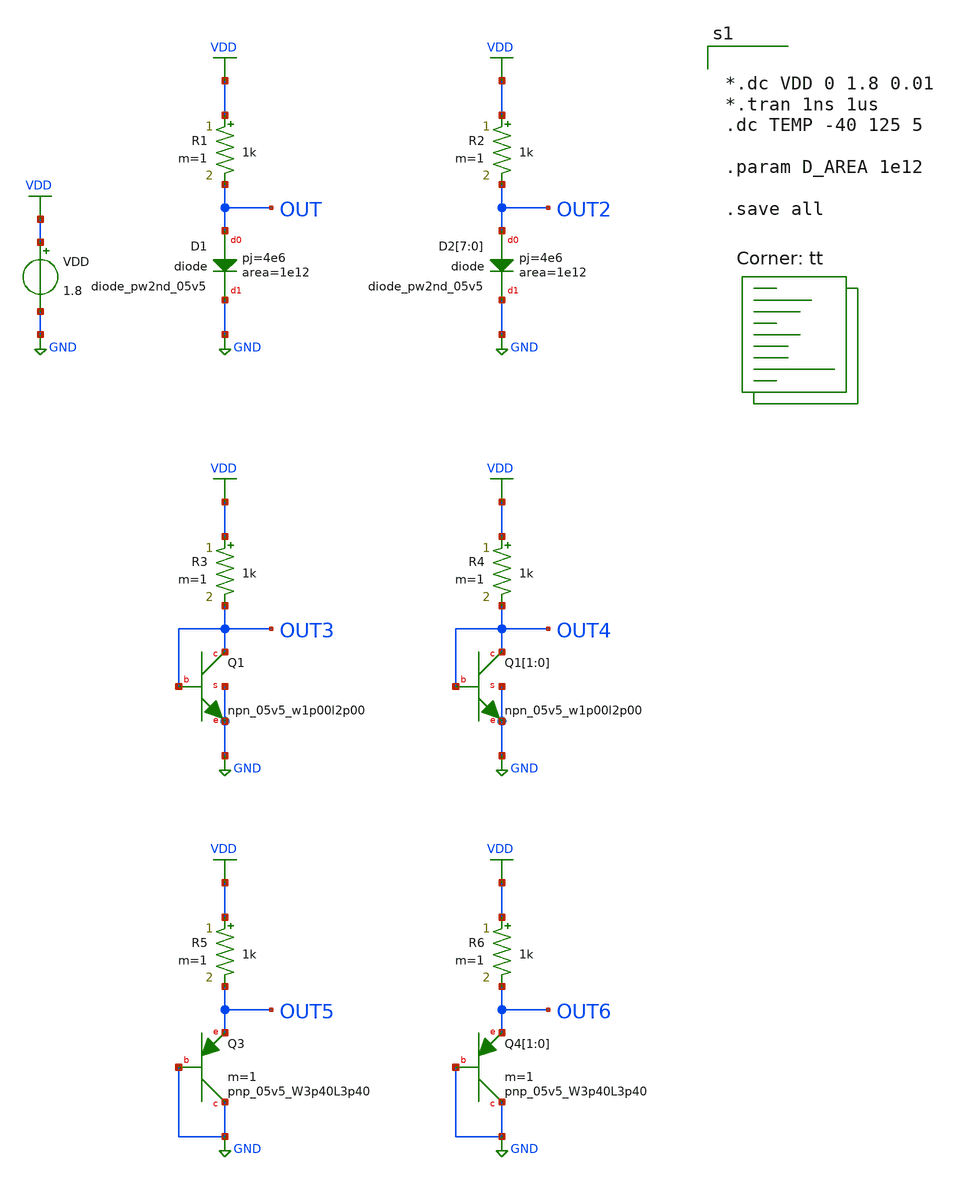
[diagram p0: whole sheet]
** sch_path: design/CNR_GR04_SKY130NM/CNR_GR04_Temp_Sweep.sch
**.subckt CNR_GR04_Temp_Sweep
XD1 OUT GND sky130_fd_pr__diode_pw2nd_05v5 area=1e12 pj=4e6
R1 VDD OUT 1k m=1
VDD VDD GND 1.8
XD2[7] OUT2 GND sky130_fd_pr__diode_pw2nd_05v5 area=1e12 pj=4e6
XD2[6] OUT2 GND sky130_fd_pr__diode_pw2nd_05v5 area=1e12 pj=4e6
XD2[5] OUT2 GND sky130_fd_pr__diode_pw2nd_05v5 area=1e12 pj=4e6
XD2[4] OUT2 GND sky130_fd_pr__diode_pw2nd_05v5 area=1e12 pj=4e6
XD2[3] OUT2 GND sky130_fd_pr__diode_pw2nd_05v5 area=1e12 pj=4e6
XD2[2] OUT2 GND sky130_fd_pr__diode_pw2nd_05v5 area=1e12 pj=4e6
XD2[1] OUT2 GND sky130_fd_pr__diode_pw2nd_05v5 area=1e12 pj=4e6
XD2[0] OUT2 GND sky130_fd_pr__diode_pw2nd_05v5 area=1e12 pj=4e6
R2 VDD OUT2 1k m=1
XQ1 OUT3 OUT3 GND GND sky130_fd_pr__npn_05v5_w1p00l2p00
R3 VDD OUT3 1k m=1
R4 VDD OUT4 1k m=1
XQ1[1] OUT4 OUT4 GND GND sky130_fd_pr__npn_05v5_w1p00l2p00
XQ1[0] OUT4 OUT4 GND GND sky130_fd_pr__npn_05v5_w1p00l2p00
R5 VDD OUT5 1k m=1
R6 VDD OUT6 1k m=1
XQ3 GND GND OUT5 sky130_fd_pr__pnp_05v5_W3p40L3p40 m=1
XQ4[1] GND GND OUT6 sky130_fd_pr__pnp_05v5_W3p40L3p40 m=1
XQ4[0] GND GND OUT6 sky130_fd_pr__pnp_05v5_W3p40L3p40 m=1
**** begin user architecture code


*.dc VDD 0 1.8 0.01
*.tran 1ns 1us
.dc TEMP -40 125 5

.param D_AREA 1e12

.save all



.lib $::SKYWATER_MODELS/sky130.lib.spice tt
**** end user architecture code
**.ends
.GLOBAL GND
.GLOBAL VDD
.end
